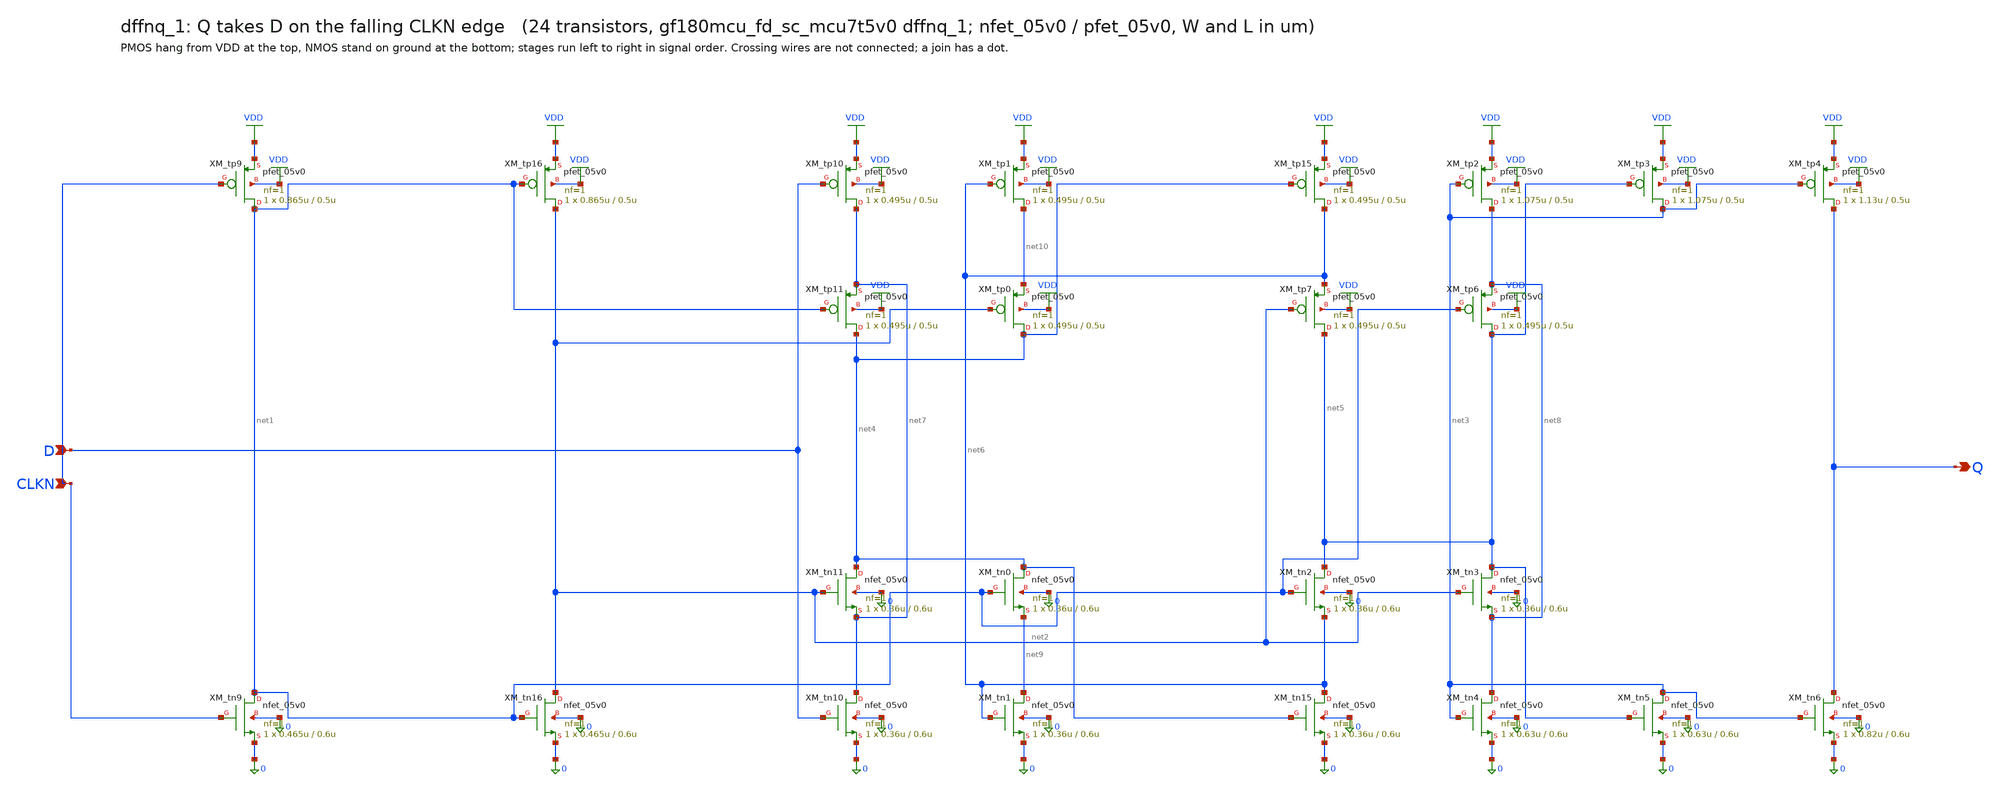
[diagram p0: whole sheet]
** sch_path: xschem/cells_tx/dffnq_1.sch
**.subckt dffnq_1 D CLKN Q
*.ipin D
*.ipin CLKN
*.opin Q
XM_tn9 net1 CLKN 0 0 nfet_05v0 L=0.6u W=0.465u nf=1 ad=2.325e-13 as=2.325e-13 pd=1.93e-06
+ ps=1.93e-06 nrd=0 nrs=0 sa=0 sb=0 sd=0 m=1
XM_tn16 net2 net1 0 0 nfet_05v0 L=0.6u W=0.465u nf=1 ad=2.325e-13 as=2.325e-13 pd=1.93e-06
+ ps=1.93e-06 nrd=0 nrs=0 sa=0 sb=0 sd=0 m=1
XM_tn10 net7 D 0 0 nfet_05v0 L=0.6u W=0.36u nf=1 ad=1.8e-13 as=1.8e-13 pd=1.72e-06 ps=1.72e-06 nrd=0
+ nrs=0 sa=0 sb=0 sd=0 m=1
XM_tn11 net4 net2 net7 0 nfet_05v0 L=0.6u W=0.36u nf=1 ad=1.8e-13 as=1.8e-13 pd=1.72e-06 ps=1.72e-06
+ nrd=0 nrs=0 sa=0 sb=0 sd=0 m=1
XM_tn0 net4 net1 net9 0 nfet_05v0 L=0.6u W=0.36u nf=1 ad=1.8e-13 as=1.8e-13 pd=1.72e-06 ps=1.72e-06
+ nrd=0 nrs=0 sa=0 sb=0 sd=0 m=1
XM_tn1 net9 net6 0 0 nfet_05v0 L=0.6u W=0.36u nf=1 ad=1.8e-13 as=1.8e-13 pd=1.72e-06 ps=1.72e-06
+ nrd=0 nrs=0 sa=0 sb=0 sd=0 m=1
XM_tn15 net6 net4 0 0 nfet_05v0 L=0.6u W=0.36u nf=1 ad=1.8e-13 as=1.8e-13 pd=1.72e-06 ps=1.72e-06
+ nrd=0 nrs=0 sa=0 sb=0 sd=0 m=1
XM_tn2 net5 net1 net6 0 nfet_05v0 L=0.6u W=0.36u nf=1 ad=1.8e-13 as=1.8e-13 pd=1.72e-06 ps=1.72e-06
+ nrd=0 nrs=0 sa=0 sb=0 sd=0 m=1
XM_tn3 net5 net2 net8 0 nfet_05v0 L=0.6u W=0.36u nf=1 ad=1.8e-13 as=1.8e-13 pd=1.72e-06 ps=1.72e-06
+ nrd=0 nrs=0 sa=0 sb=0 sd=0 m=1
XM_tn4 net8 net3 0 0 nfet_05v0 L=0.6u W=0.63u nf=1 ad=3.15e-13 as=3.15e-13 pd=2.26e-06 ps=2.26e-06
+ nrd=0 nrs=0 sa=0 sb=0 sd=0 m=1
XM_tn5 net3 net5 0 0 nfet_05v0 L=0.6u W=0.63u nf=1 ad=3.15e-13 as=3.15e-13 pd=2.26e-06 ps=2.26e-06
+ nrd=0 nrs=0 sa=0 sb=0 sd=0 m=1
XM_tn6 Q net3 0 0 nfet_05v0 L=0.6u W=0.82u nf=1 ad=4.1e-13 as=4.1e-13 pd=2.64e-06 ps=2.64e-06 nrd=0
+ nrs=0 sa=0 sb=0 sd=0 m=1
XM_tp9 net1 CLKN VDD VDD pfet_05v0 L=0.5u W=0.865u nf=1 ad=4.325e-13 as=4.325e-13 pd=2.73e-06
+ ps=2.73e-06 nrd=0 nrs=0 sa=0 sb=0 sd=0 m=1
XM_tp16 net2 net1 VDD VDD pfet_05v0 L=0.5u W=0.865u nf=1 ad=4.325e-13 as=4.325e-13 pd=2.73e-06
+ ps=2.73e-06 nrd=0 nrs=0 sa=0 sb=0 sd=0 m=1
XM_tp10 net7 D VDD VDD pfet_05v0 L=0.5u W=0.495u nf=1 ad=2.475e-13 as=2.475e-13 pd=1.99e-06
+ ps=1.99e-06 nrd=0 nrs=0 sa=0 sb=0 sd=0 m=1
XM_tp11 net4 net1 net7 VDD pfet_05v0 L=0.5u W=0.495u nf=1 ad=2.475e-13 as=2.475e-13 pd=1.99e-06
+ ps=1.99e-06 nrd=0 nrs=0 sa=0 sb=0 sd=0 m=1
XM_tp0 net4 net2 net10 VDD pfet_05v0 L=0.5u W=0.495u nf=1 ad=2.475e-13 as=2.475e-13 pd=1.99e-06
+ ps=1.99e-06 nrd=0 nrs=0 sa=0 sb=0 sd=0 m=1
XM_tp1 net10 net6 VDD VDD pfet_05v0 L=0.5u W=0.495u nf=1 ad=2.475e-13 as=2.475e-13 pd=1.99e-06
+ ps=1.99e-06 nrd=0 nrs=0 sa=0 sb=0 sd=0 m=1
XM_tp15 net6 net4 VDD VDD pfet_05v0 L=0.5u W=0.495u nf=1 ad=2.475e-13 as=2.475e-13 pd=1.99e-06
+ ps=1.99e-06 nrd=0 nrs=0 sa=0 sb=0 sd=0 m=1
XM_tp7 net5 net2 net6 VDD pfet_05v0 L=0.5u W=0.495u nf=1 ad=2.475e-13 as=2.475e-13 pd=1.99e-06
+ ps=1.99e-06 nrd=0 nrs=0 sa=0 sb=0 sd=0 m=1
XM_tp6 net5 net1 net8 VDD pfet_05v0 L=0.5u W=0.495u nf=1 ad=2.475e-13 as=2.475e-13 pd=1.99e-06
+ ps=1.99e-06 nrd=0 nrs=0 sa=0 sb=0 sd=0 m=1
XM_tp2 net8 net3 VDD VDD pfet_05v0 L=0.5u W=1.075u nf=1 ad=5.375e-13 as=5.375e-13 pd=3.15e-06
+ ps=3.15e-06 nrd=0 nrs=0 sa=0 sb=0 sd=0 m=1
XM_tp3 net3 net5 VDD VDD pfet_05v0 L=0.5u W=1.075u nf=1 ad=5.375e-13 as=5.375e-13 pd=3.15e-06
+ ps=3.15e-06 nrd=0 nrs=0 sa=0 sb=0 sd=0 m=1
XM_tp4 Q net3 VDD VDD pfet_05v0 L=0.5u W=1.13u nf=1 ad=5.65e-13 as=5.65e-13 pd=3.26e-06 ps=3.26e-06
+ nrd=0 nrs=0 sa=0 sb=0 sd=0 m=1
**.ends
.GLOBAL VDD
.end
